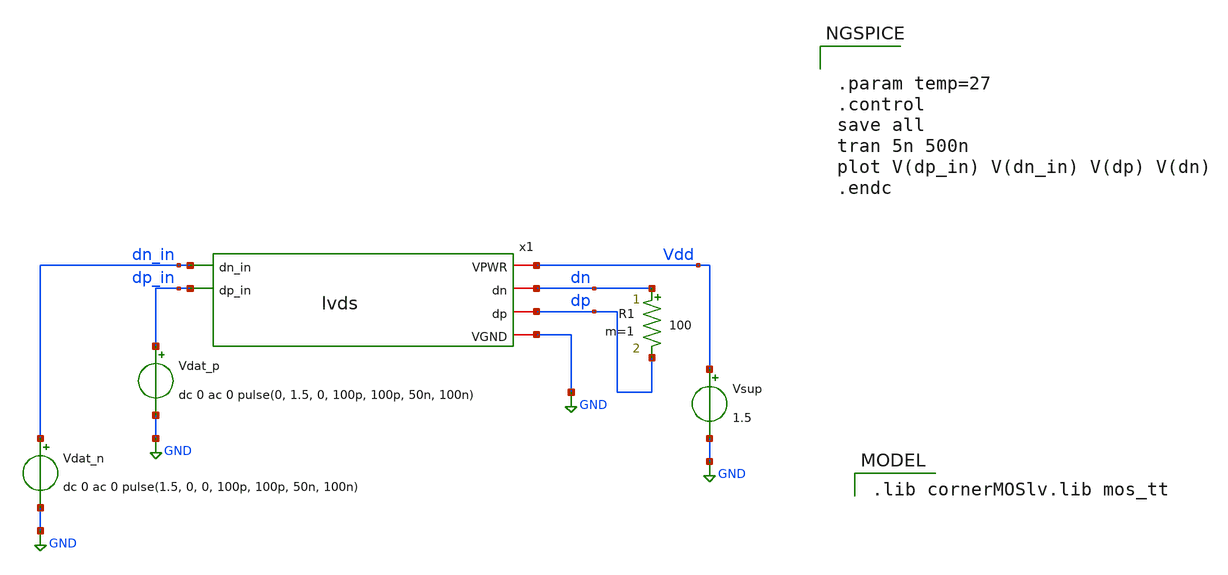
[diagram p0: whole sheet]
** sch_path: xschem/lvds_tb.sch
**.subckt lvds_tb
Vsup Vdd GND 1.5
Vdat_p dp_in GND dc 0 ac 0 pulse(0, 1.5, 0, 100p, 100p, 50n, 100n)
Vdat_n dn_in GND dc 0 ac 0 pulse(1.5, 0, 0, 100p, 100p, 50n, 100n)
R1 dn dp 100 m=1
x1 Vdd dn dn_in dp dp_in GND lvds
**** begin user architecture code
 .lib cornerMOSlv.lib mos_tt



.param temp=27
.control
save all
tran 5n 500n
plot V(dp_in) V(dn_in) V(dp) V(dn)
.endc


**** end user architecture code
**.ends

* expanding   symbol:  /home/pc/heichips25-ethernet/xschem/lvds.sym # of pins=6
** sym_path: xschem/lvds.sym
** sch_path: xschem/lvds.sch
.subckt lvds VPWR dn dn_in dp dp_in VGND
*.ipin dp_in
*.ipin dn_in
*.iopin VPWR
*.iopin VGND
*.iopin dp
*.iopin dn
XM1 dp dp_in net1 net1 sg13_lv_nmos w=50u l=1u ng=5 m=1 mm_ok=1
XM2 dn dn_in net1 net1 sg13_lv_nmos w=50u l=1u ng=5 m=1 mm_ok=1
XM5 dp dp_in VPWR VPWR sg13_lv_pmos w=50u l=1u ng=5 m=1 mm_ok=1
XM6 dn dn_in VPWR VPWR sg13_lv_pmos w=50u l=1u ng=5 m=1 mm_ok=1
XM3 net1 net2 VGND VGND sg13_lv_nmos w=50u l=1u ng=5 m=1 mm_ok=1
XM4 net2 net2 VGND VGND sg13_lv_nmos w=10u l=4u ng=1 m=1 mm_ok=1
XM7 VPWR VPWR net2 net2 sg13_lv_nmos w=10u l=10u ng=1 m=1 mm_ok=1
.ends

.GLOBAL GND
.end
